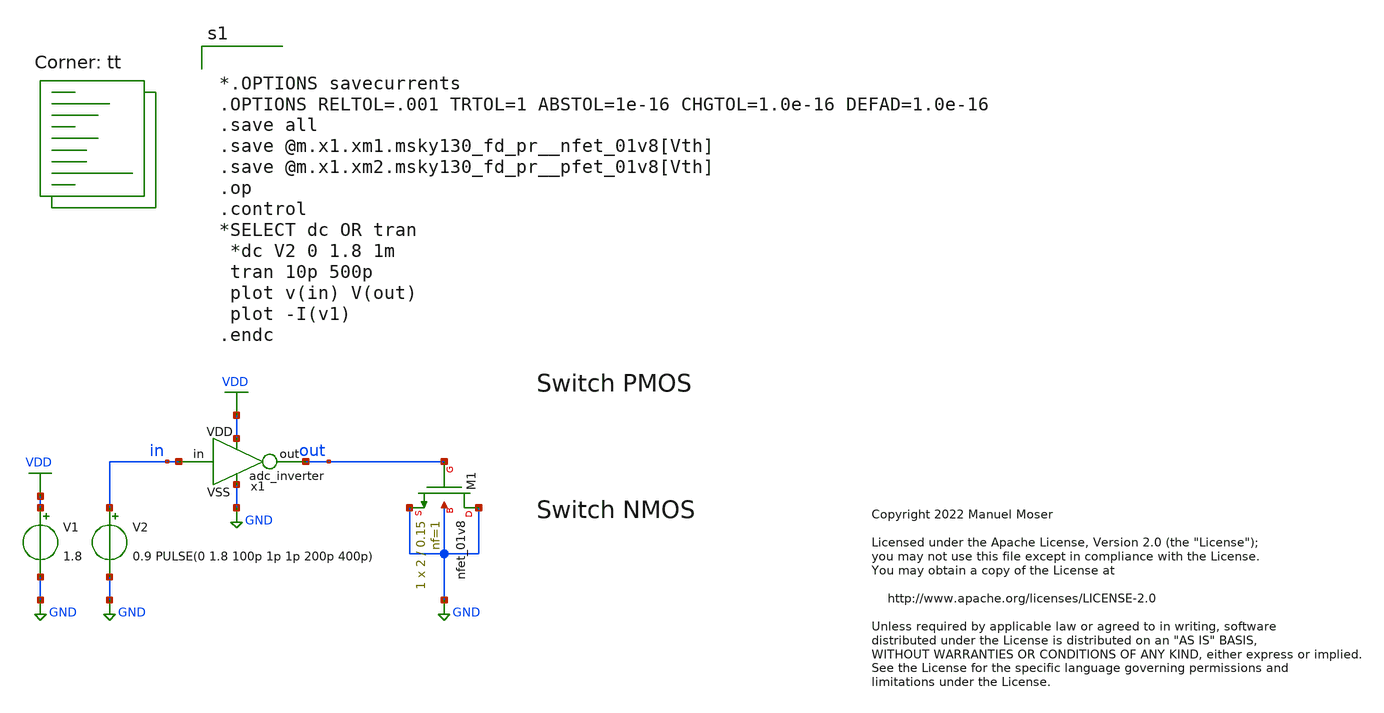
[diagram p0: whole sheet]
** sch_path: xschem/adc_inverter_tb.sch
* Copyright 2022 Manuel Moser
* Licensed under the Apache License, Version 2.0 (the "License");
**.subckt adc_inverter_tb
V1 VDD GND 1.8
V2 in GND 0.9 PULSE(0 1.8 100p 1p 1p 200p 400p)
XM1 GND out GND GND sky130_fd_pr__nfet_01v8 L=0.15 W=2 nf=1 ad='int((nf+1)/2) * W/nf * 0.29' as='int((nf+2)/2) * W/nf * 0.29'
+ pd='2*int((nf+1)/2) * (W/nf + 0.29)' ps='2*int((nf+2)/2) * (W/nf + 0.29)' nrd='0.29 / W' nrs='0.29 / W'
+ sa=0 sb=0 sd=0 mult=1 m=1
x1 VDD GND in out adc_inverter
**** begin user architecture code


*.OPTIONS savecurrents
.OPTIONS RELTOL=.001 TRTOL=1 ABSTOL=1e-16 CHGTOL=1.0e-16 DEFAD=1.0e-16
.save all
.save @m.x1.xm1.msky130_fd_pr__nfet_01v8[Vth]
.save @m.x1.xm2.msky130_fd_pr__pfet_01v8[Vth]
.op
.control
*SELECT dc OR tran
 *dc V2 0 1.8 1m
 tran 10p 500p
 plot v(in) V(out)
 plot -I(v1)
.endc


.lib $::SKYWATER_MODELS/sky130.lib.spice tt
**** end user architecture code
**.ends

* expanding   symbol:  adc_inverter.sym # of pins=4
** sym_path: xschem/adc_inverter.sym
** sch_path: xschem/adc_inverter.sch
.subckt adc_inverter VDD VSS in out
*.iopin VDD
*.iopin VSS
*.opin out
*.ipin in
XM1 out in VSS VSS sky130_fd_pr__nfet_01v8 L=0.15 W=0.42 nf=1 ad='int((nf+1)/2) * W/nf * 0.29' as='int((nf+2)/2) * W/nf * 0.29'
+ pd='2*int((nf+1)/2) * (W/nf + 0.29)' ps='2*int((nf+2)/2) * (W/nf + 0.29)' nrd='0.29 / W' nrs='0.29 / W'
+ sa=0 sb=0 sd=0 mult=1 m=1
XM2 out in VDD VDD sky130_fd_pr__pfet_01v8 L=0.15 W=0.84 nf=2 ad='int((nf+1)/2) * W/nf * 0.29' as='int((nf+2)/2) * W/nf * 0.29'
+ pd='2*int((nf+1)/2) * (W/nf + 0.29)' ps='2*int((nf+2)/2) * (W/nf + 0.29)' nrd='0.29 / W' nrs='0.29 / W'
+ sa=0 sb=0 sd=0 mult=1 m=1
.ends

.GLOBAL GND
.GLOBAL VDD
.end
